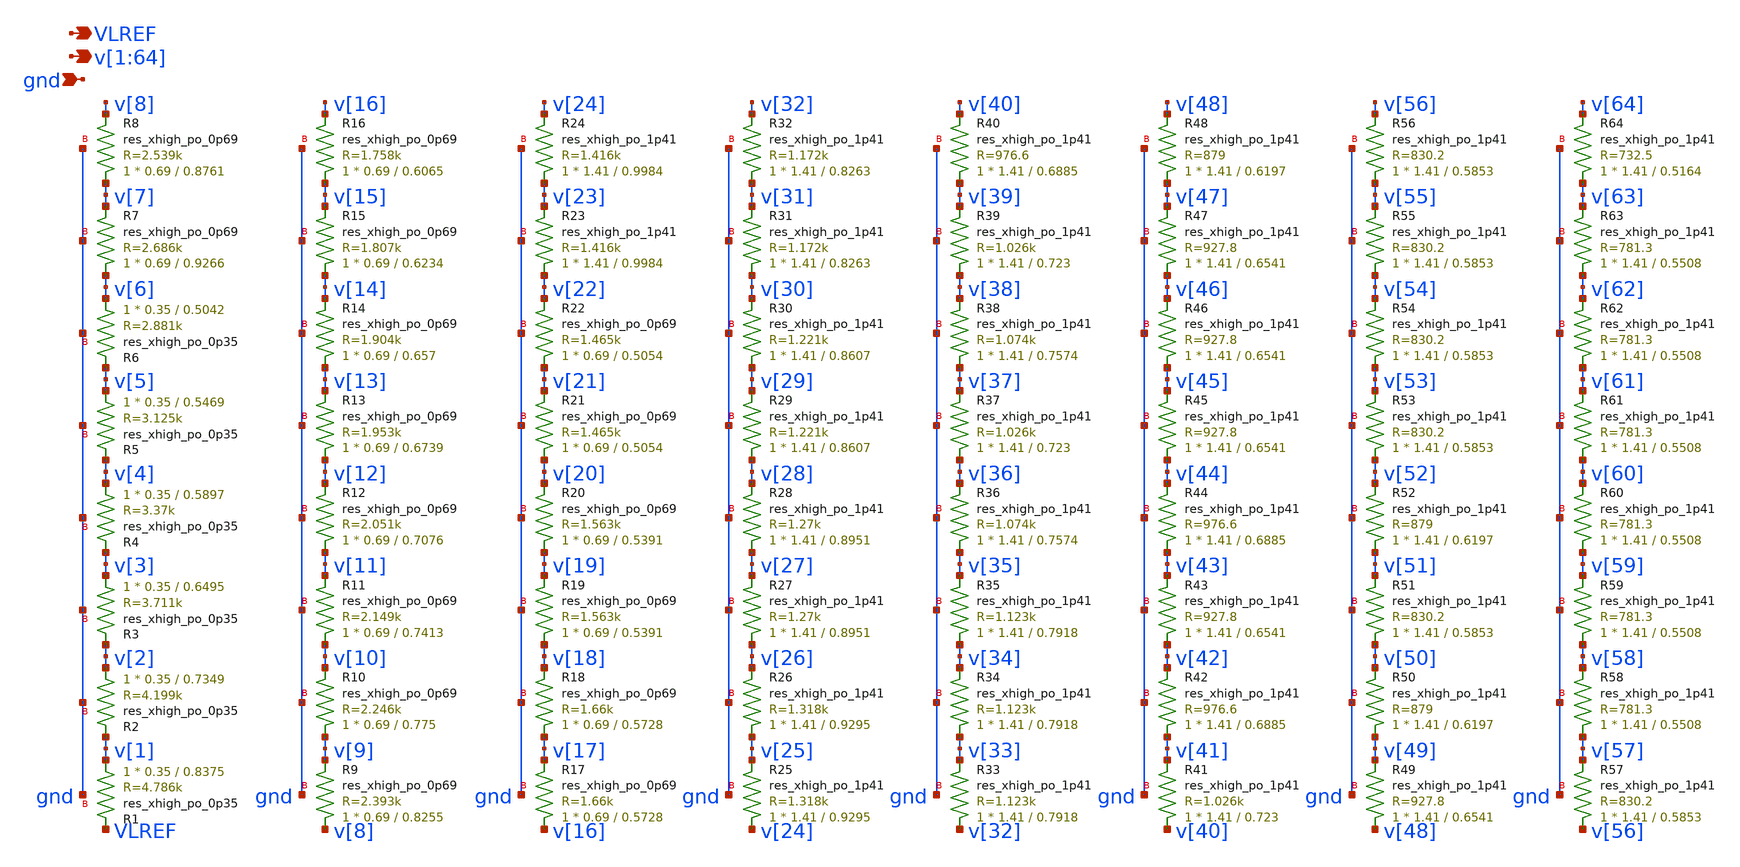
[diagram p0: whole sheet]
** sch_path: xschem/res_seg_1.sch
**.subckt res_seg_1
*+ v[1],v[2],v[3],v[4],v[5],v[6],v[7],v[8],v[9],v[10],v[11],v[12],v[13],v[14],v[15],v[16],v[17],v[18],v[19],v[20],v[21],v[22],v[23],v[24],v[25],v[26],v[27],v[28],v[29],v[30],v[31],v[32],v[33],v[34],v[35],v[36],v[37],v[38],v[39],v[40],v[41],v[42],v[43],v[44],v[45],v[46],v[47],v[48],v[49],v[50],v[51],v[52],v[53],v[54],v[55],v[56],v[57],v[58],v[59],v[60],v[61],v[62],v[63],v[64] gnd VLREF
*.opin
*+ v[1],v[2],v[3],v[4],v[5],v[6],v[7],v[8],v[9],v[10],v[11],v[12],v[13],v[14],v[15],v[16],v[17],v[18],v[19],v[20],v[21],v[22],v[23],v[24],v[25],v[26],v[27],v[28],v[29],v[30],v[31],v[32],v[33],v[34],v[35],v[36],v[37],v[38],v[39],v[40],v[41],v[42],v[43],v[44],v[45],v[46],v[47],v[48],v[49],v[50],v[51],v[52],v[53],v[54],v[55],v[56],v[57],v[58],v[59],v[60],v[61],v[62],v[63],v[64]
*.ipin gnd
*.opin VLREF
XR1 v[1] VLREF gnd sky130_fd_pr__res_xhigh_po_0p35 L=0.8375 mult=1 m=1
XR2 v[2] v[1] gnd sky130_fd_pr__res_xhigh_po_0p35 L=0.7349 mult=1 m=1
XR3 v[3] v[2] gnd sky130_fd_pr__res_xhigh_po_0p35 L=0.6495 mult=1 m=1
XR4 v[4] v[3] gnd sky130_fd_pr__res_xhigh_po_0p35 L=0.5897 mult=1 m=1
XR8 v[7] v[8] gnd sky130_fd_pr__res_xhigh_po_0p69 L=0.8761 mult=1 m=1
XR9 v[8] v[9] gnd sky130_fd_pr__res_xhigh_po_0p69 L=0.8255 mult=1 m=1
XR10 v[9] v[10] gnd sky130_fd_pr__res_xhigh_po_0p69 L=0.775 mult=1 m=1
XR11 v[10] v[11] gnd sky130_fd_pr__res_xhigh_po_0p69 L=0.7413 mult=1 m=1
XR12 v[11] v[12] gnd sky130_fd_pr__res_xhigh_po_0p69 L=0.7076 mult=1 m=1
XR13 v[12] v[13] gnd sky130_fd_pr__res_xhigh_po_0p69 L=0.6739 mult=1 m=1
XR14 v[13] v[14] gnd sky130_fd_pr__res_xhigh_po_0p69 L=0.657 mult=1 m=1
XR15 v[14] v[15] gnd sky130_fd_pr__res_xhigh_po_0p69 L=0.6234 mult=1 m=1
XR16 v[15] v[16] gnd sky130_fd_pr__res_xhigh_po_0p69 L=0.6065 mult=1 m=1
XR17 v[16] v[17] gnd sky130_fd_pr__res_xhigh_po_0p69 L=0.5728 mult=1 m=1
XR19 v[18] v[19] gnd sky130_fd_pr__res_xhigh_po_0p69 L=0.5391 mult=1 m=1
XR27 v[26] v[27] gnd sky130_fd_pr__res_xhigh_po_1p41 L=0.8951 mult=1 m=1
XR29 v[28] v[29] gnd sky130_fd_pr__res_xhigh_po_1p41 L=0.8607 mult=1 m=1
XR31 v[30] v[31] gnd sky130_fd_pr__res_xhigh_po_1p41 L=0.8263 mult=1 m=1
XR33 v[32] v[33] gnd sky130_fd_pr__res_xhigh_po_1p41 L=0.7918 mult=1 m=1
XR36 v[35] v[36] gnd sky130_fd_pr__res_xhigh_po_1p41 L=0.7574 mult=1 m=1
XR37 v[36] v[37] gnd sky130_fd_pr__res_xhigh_po_1p41 L=0.723 mult=1 m=1
XR40 v[39] v[40] gnd sky130_fd_pr__res_xhigh_po_1p41 L=0.6885 mult=1 m=1
XR41 v[40] v[41] gnd sky130_fd_pr__res_xhigh_po_1p41 L=0.723 mult=1 m=1
XR42 v[41] v[42] gnd sky130_fd_pr__res_xhigh_po_1p41 L=0.6885 mult=1 m=1
XR43 v[42] v[43] gnd sky130_fd_pr__res_xhigh_po_1p41 L=0.6541 mult=1 m=1
XR45 v[44] v[45] gnd sky130_fd_pr__res_xhigh_po_1p41 L=0.6541 mult=1 m=1
XR48 v[47] v[48] gnd sky130_fd_pr__res_xhigh_po_1p41 L=0.6197 mult=1 m=1
XR49 v[48] v[49] gnd sky130_fd_pr__res_xhigh_po_1p41 L=0.6541 mult=1 m=1
XR51 v[50] v[51] gnd sky130_fd_pr__res_xhigh_po_1p41 L=0.5853 mult=1 m=1
XR52 v[51] v[52] gnd sky130_fd_pr__res_xhigh_po_1p41 L=0.6197 mult=1 m=1
XR53 v[52] v[53] gnd sky130_fd_pr__res_xhigh_po_1p41 L=0.5853 mult=1 m=1
XR58 v[57] v[58] gnd sky130_fd_pr__res_xhigh_po_1p41 L=0.5508 mult=1 m=1
XR64 v[63] v[64] gnd sky130_fd_pr__res_xhigh_po_1p41 L=0.5164 mult=1 m=1
XR5 v[5] v[4] gnd sky130_fd_pr__res_xhigh_po_0p35 L=0.5469 mult=1 m=1
XR6 v[6] v[5] gnd sky130_fd_pr__res_xhigh_po_0p35 L=0.5042 mult=1 m=1
XR21 v[20] v[21] gnd sky130_fd_pr__res_xhigh_po_0p69 L=0.5054 mult=1 m=1
XR54 v[53] v[54] gnd sky130_fd_pr__res_xhigh_po_1p41 L=0.5853 mult=1 m=1
XR7 v[6] v[7] gnd sky130_fd_pr__res_xhigh_po_0p69 L=0.9266 mult=1 m=1
XR18 v[17] v[18] gnd sky130_fd_pr__res_xhigh_po_0p69 L=0.5728 mult=1 m=1
XR20 v[19] v[20] gnd sky130_fd_pr__res_xhigh_po_0p69 L=0.5391 mult=1 m=1
XR22 v[21] v[22] gnd sky130_fd_pr__res_xhigh_po_0p69 L=0.5054 mult=1 m=1
XR23 v[22] v[23] gnd sky130_fd_pr__res_xhigh_po_1p41 L=0.9984 mult=1 m=1
XR24 v[23] v[24] gnd sky130_fd_pr__res_xhigh_po_1p41 L=0.9984 mult=1 m=1
XR25 v[24] v[25] gnd sky130_fd_pr__res_xhigh_po_1p41 L=0.9295 mult=1 m=1
XR26 v[25] v[26] gnd sky130_fd_pr__res_xhigh_po_1p41 L=0.9295 mult=1 m=1
XR28 v[27] v[28] gnd sky130_fd_pr__res_xhigh_po_1p41 L=0.8951 mult=1 m=1
XR30 v[29] v[30] gnd sky130_fd_pr__res_xhigh_po_1p41 L=0.8607 mult=1 m=1
XR32 v[31] v[32] gnd sky130_fd_pr__res_xhigh_po_1p41 L=0.8263 mult=1 m=1
XR34 v[33] v[34] gnd sky130_fd_pr__res_xhigh_po_1p41 L=0.7918 mult=1 m=1
XR35 v[34] v[35] gnd sky130_fd_pr__res_xhigh_po_1p41 L=0.7918 mult=1 m=1
XR38 v[37] v[38] gnd sky130_fd_pr__res_xhigh_po_1p41 L=0.7574 mult=1 m=1
XR39 v[38] v[39] gnd sky130_fd_pr__res_xhigh_po_1p41 L=0.723 mult=1 m=1
XR44 v[43] v[44] gnd sky130_fd_pr__res_xhigh_po_1p41 L=0.6885 mult=1 m=1
XR46 v[45] v[46] gnd sky130_fd_pr__res_xhigh_po_1p41 L=0.6541 mult=1 m=1
XR47 v[46] v[47] gnd sky130_fd_pr__res_xhigh_po_1p41 L=0.6541 mult=1 m=1
XR50 v[49] v[50] gnd sky130_fd_pr__res_xhigh_po_1p41 L=0.6197 mult=1 m=1
XR55 v[54] v[55] gnd sky130_fd_pr__res_xhigh_po_1p41 L=0.5853 mult=1 m=1
XR56 v[55] v[56] gnd sky130_fd_pr__res_xhigh_po_1p41 L=0.5853 mult=1 m=1
XR57 v[56] v[57] gnd sky130_fd_pr__res_xhigh_po_1p41 L=0.5853 mult=1 m=1
XR59 v[58] v[59] gnd sky130_fd_pr__res_xhigh_po_1p41 L=0.5508 mult=1 m=1
XR60 v[59] v[60] gnd sky130_fd_pr__res_xhigh_po_1p41 L=0.5508 mult=1 m=1
XR61 v[60] v[61] gnd sky130_fd_pr__res_xhigh_po_1p41 L=0.5508 mult=1 m=1
XR62 v[61] v[62] gnd sky130_fd_pr__res_xhigh_po_1p41 L=0.5508 mult=1 m=1
XR63 v[62] v[63] gnd sky130_fd_pr__res_xhigh_po_1p41 L=0.5508 mult=1 m=1
**.ends
.end
